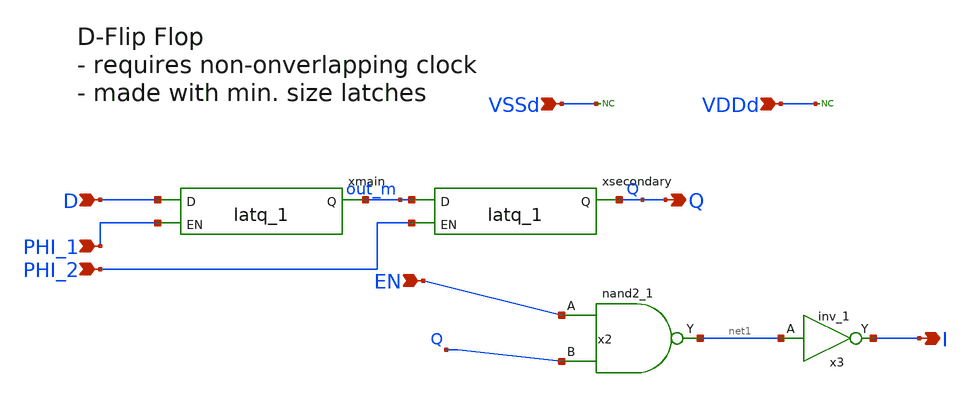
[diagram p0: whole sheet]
** sch_path: designs/libs/core_swmatrix/DFF_2phase_1.sch
**.subckt DFF_2phase_1 D PHI_1 PHI_2 Q EN I VSSd VDDd
*.ipin D
*.ipin PHI_1
*.ipin PHI_2
*.opin Q
*.ipin EN
*.opin I
*.ipin VSSd
*.ipin VDDd
xmain D PHI_1 out_m VDDd VDDd VSSd VSSd gf180mcu_fd_sc_mcu9t5v0__latq_1
xsecondary out_m PHI_2 Q VDDd VDDd VSSd VSSd gf180mcu_fd_sc_mcu9t5v0__latq_1
x2 EN Q VSSd VDDd VSSd VDDd net1 gf180mcu_fd_sc_mcu9t5v0__nand2_1
x3 net1 VSSd VDDd VSSd VDDd I gf180mcu_fd_sc_mcu9t5v0__inv_1
* noconn VSSd
* noconn VDDd
**.ends
.end
